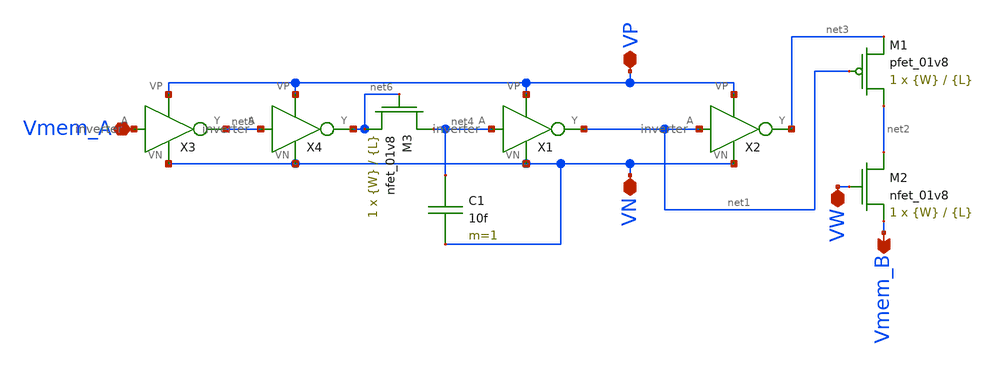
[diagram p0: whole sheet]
** sch_path: schematic/switched_artificial_synapse.sch
**.subckt switched_artificial_synapse VP VN VW Vmem_A Vmem_B
*.iopin VP
*.iopin VN
*.iopin VW
*.iopin Vmem_A
*.opin Vmem_B
X1 net4 VN VP net1 inverter
X2 net1 VN VP net3 inverter
XM1 net2 net1 net3 VDD sky130_fd_pr__pfet_01v8 L={L} W={W} nf=1 ad='int((nf+1)/2) * W/nf * 0.29' as='int((nf+2)/2) * W/nf * 0.29'
+ pd='2*int((nf+1)/2) * (W/nf + 0.29)' ps='2*int((nf+2)/2) * (W/nf + 0.29)' nrd='0.29 / W' nrs='0.29 / W'
+ sa=0 sb=0 sd=0 mult=1 m=1
XM2 net2 VW Vmem_B GND sky130_fd_pr__nfet_01v8 L={L} W={W} nf=1 ad='int((nf+1)/2) * W/nf * 0.29' as='int((nf+2)/2) * W/nf * 0.29'
+ pd='2*int((nf+1)/2) * (W/nf + 0.29)' ps='2*int((nf+2)/2) * (W/nf + 0.29)' nrd='0.29 / W' nrs='0.29 / W'
+ sa=0 sb=0 sd=0 mult=1 m=1
X3 Vmem_A VN VP net5 inverter
X4 net5 VN VP net6 inverter
XM3 net4 net6 net6 GND sky130_fd_pr__nfet_01v8 L={L} W={W} nf=1 ad='int((nf+1)/2) * W/nf * 0.29' as='int((nf+2)/2) * W/nf * 0.29'
+ pd='2*int((nf+1)/2) * (W/nf + 0.29)' ps='2*int((nf+2)/2) * (W/nf + 0.29)' nrd='0.29 / W' nrs='0.29 / W'
+ sa=0 sb=0 sd=0 mult=1 m=1
C1 net4 VN 10f m=1
**.ends

* expanding   symbol:  /home/madvlsi/neuromorphic_computing_final/schematic/inverter.sym # of pins=4
** sym_path: schematic/inverter.sym
** sch_path: schematic/inverter.sch
.subckt inverter A VN VP Y
*.ipin A
*.iopin VP
*.iopin VN
*.opin Y
XM1 Y A VN VN sky130_fd_pr__nfet_01v8 L=0.15 W=1 nf=1 ad='int((nf+1)/2) * W/nf * 0.29' as='int((nf+2)/2) * W/nf * 0.29'
+ pd='2*int((nf+1)/2) * (W/nf + 0.29)' ps='2*int((nf+2)/2) * (W/nf + 0.29)' nrd='0.29 / W' nrs='0.29 / W'
+ sa=0 sb=0 sd=0 mult=1 m=1
XM2 Y A VP VP sky130_fd_pr__pfet_01v8 L=0.15 W=1 nf=1 ad='int((nf+1)/2) * W/nf * 0.29' as='int((nf+2)/2) * W/nf * 0.29'
+ pd='2*int((nf+1)/2) * (W/nf + 0.29)' ps='2*int((nf+2)/2) * (W/nf + 0.29)' nrd='0.29 / W' nrs='0.29 / W'
+ sa=0 sb=0 sd=0 mult=1 m=1
.ends

.end
